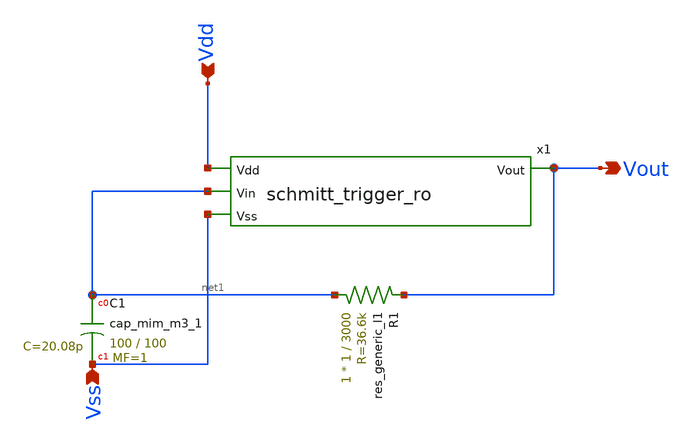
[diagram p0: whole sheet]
** sch_path: custom_gds/tt_um_test_commit/xschem/relax_osc.sch
**.subckt relax_osc Vss Vdd Vout
*.ipin Vss
*.ipin Vdd
*.opin Vout
R1 net1 Vout sky130_fd_pr__res_generic_l1 W=1 L=3000 m=1
XC1 net1 Vss sky130_fd_pr__cap_mim_m3_1 W=100 L=100 MF=1 m=1
x1 Vdd net1 Vout Vss schmitt_trigger_ro
**.ends

* expanding   symbol:  schmitt_trigger_ro.sym # of pins=4
** sym_path: custom_gds/tt_um_test_commit/xschem/schmitt_trigger_ro.sym
** sch_path: custom_gds/tt_um_test_commit/xschem/schmitt_trigger_ro.sch
.subckt schmitt_trigger_ro Vdd Vin Vout Vss
*.ipin Vdd
*.ipin Vss
*.ipin Vin
*.opin Vout
XM10 net1 Vin Vdd Vdd sky130_fd_pr__pfet_01v8_lvt L=0.35 W=6 nf=1 ad='int((1 + 1)/2) * 6 / 1 * 0.29'
+ as='int((1 + 2)/2) * 6 / 1 * 0.29' pd='2*int((1 + 1)/2) * (6 / 1 + 0.29)' ps='2*int((1 + 2)/2) * (6 / 1 + 0.29)'
+ nrd='0.29 / 6 ' nrs='0.29 / 6 ' sa=0 sb=0 sd=0 mult=1 m=1
XM2 Vout Vin net1 Vdd sky130_fd_pr__pfet_01v8_lvt L=0.35 W=6 nf=1 ad='int((1 + 1)/2) * 6 / 1 * 0.29'
+ as='int((1 + 2)/2) * 6 / 1 * 0.29' pd='2*int((1 + 1)/2) * (6 / 1 + 0.29)' ps='2*int((1 + 2)/2) * (6 / 1 + 0.29)'
+ nrd='0.29 / 6 ' nrs='0.29 / 6 ' sa=0 sb=0 sd=0 mult=1 m=1
XM4 net3 Vout net1 Vdd sky130_fd_pr__pfet_01v8_lvt L=0.35 W=6 nf=1 ad='int((1 + 1)/2) * 6 / 1 * 0.29'
+ as='int((1 + 2)/2) * 6 / 1 * 0.29' pd='2*int((1 + 1)/2) * (6 / 1 + 0.29)' ps='2*int((1 + 2)/2) * (6 / 1 + 0.29)'
+ nrd='0.29 / 6 ' nrs='0.29 / 6 ' sa=0 sb=0 sd=0 mult=1 m=1
XM6 Vout Vin net2 Vss sky130_fd_pr__nfet_01v8_lvt L=0.15 W=2 nf=1 ad='int((1 + 1)/2) * 2 / 1 * 0.29'
+ as='int((1 + 2)/2) * 2 / 1 * 0.29' pd='2*int((1 + 1)/2) * (2 / 1 + 0.29)' ps='2*int((1 + 2)/2) * (2 / 1 + 0.29)'
+ nrd='0.29 / 2 ' nrs='0.29 / 2 ' sa=0 sb=0 sd=0 mult=1 m=1
XM1 net2 Vin Vss Vss sky130_fd_pr__nfet_01v8_lvt L=0.15 W=2 nf=1 ad='int((1 + 1)/2) * 2 / 1 * 0.29' as='int((1 + 2)/2) * 2 / 1 * 0.29'
+ pd='2*int((1 + 1)/2) * (2 / 1 + 0.29)' ps='2*int((1 + 2)/2) * (2 / 1 + 0.29)' nrd='0.29 / 2 ' nrs='0.29 / 2 '
+ sa=0 sb=0 sd=0 mult=1 m=1
XM3 Vdd Vout net2 Vss sky130_fd_pr__nfet_01v8_lvt L=0.15 W=2 nf=1 ad='int((1 + 1)/2) * 2 / 1 * 0.29'
+ as='int((1 + 2)/2) * 2 / 1 * 0.29' pd='2*int((1 + 1)/2) * (2 / 1 + 0.29)' ps='2*int((1 + 2)/2) * (2 / 1 + 0.29)'
+ nrd='0.29 / 2 ' nrs='0.29 / 2 ' sa=0 sb=0 sd=0 mult=1 m=1
.ends

.end
